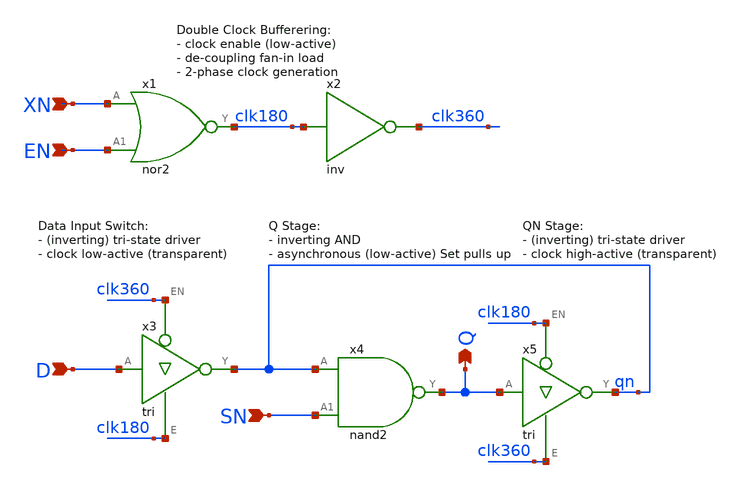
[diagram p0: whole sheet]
** sch_path: Sources/crafted/LATESN.sch
**.subckt LATESN XN D Q EN SN
*.ipin XN
*.ipin D
*.opin Q
*.ipin EN
*.ipin SN
x2 clk180 clk360 VDD GND inv Wmin=1.5u Lmin=1u g=2 m=1
x3 D clk360 clk180 qn VDD GND tri Wmin=1.5u Lmin=1u g=2 m=1
x5 Q clk180 clk360 qn VDD GND tri Wmin=1.5u Lmin=1u g=2 m=1
x1 clk180 XN EN VDD GND nor2 Wmin=1.5u Lmin=1u g=2 m=1
x4 Q qn SN VDD GND nand2 Wmin=1.5u Lmin=1u g=2 m=1
**.ends

* expanding   symbol:  inv.sym # of pins=2
** sym_path: Sources/crafted/inv.sym
** sch_path: Sources/crafted/inv.sch
.subckt inv A Y VDD GND    Wmin=1.5u Lmin=1u g=2
*.ipin A
*.opin Y
m2 Y A GND GND nmos4 w=Wmin l=Lmin m=m
m1 Y A VDD VDD pmos4 w='g*Wmin' l=Lmin m=m
.ends


* expanding   symbol:  tri.sym # of pins=4
** sym_path: Sources/crafted/tri.sym
** sch_path: Sources/crafted/tri.sch
.subckt tri A EN E Y VDD GND    Wmin=1.5u Lmin=1u g=2
*.ipin A
*.iopin Y
*.ipin EN
*.ipin E
m2 Y A net2 GND nmos4 w='2*Wmin' l=Lmin m=m
m1 Y A net1 VDD pmos4 w='2*g*Wmin' l=Lmin m=m
m0 net2 E GND GND nmos4 w='2*Wmin' l=Lmin m=m
m3 net1 EN VDD VDD pmos4 w='2*g*Wmin' l=Lmin m=m
.ends


* expanding   symbol:  nor2.sym # of pins=3
** sym_path: Sources/crafted/nor2.sym
** sch_path: Sources/crafted/nor2.sch
.subckt nor2 Y A A1 VDD GND    Wmin=1.5u Lmin=1u g=2
*.ipin A
*.opin Y
*.ipin A1
m3 Y A GND GND nmos4 w=Wmin l=Lmin m=m
m1 Y A net1 VDD pmos4 w='2*g*Wmin' l=Lmin m=m
m4 Y A1 GND GND nmos4 w=Wmin l=Lmin m=m
m2 net1 A1 VDD VDD pmos4 w='2*g*Wmin' l=Lmin m=m
.ends


* expanding   symbol:  /home/kubrick/Projects/github.com/StdCellLib/Sources/crafted/nand2.sym # of
*+ pins=3
** sym_path: Sources/crafted/nand2.sym
** sch_path: Sources/crafted/nand2.sch
.subckt nand2 Y A A1 VDD GND    Wmin=1.5u Lmin=1u g=2
*.ipin A
*.opin Y
*.ipin A1
m3 Y A net1 GND nmos4 w='2*Wmin' l=Lmin m=m
m1 Y A VDD VDD pmos4 w='g*Wmin' l=Lmin m=m
m4 net1 A1 GND GND nmos4 w='2*Wmin' l=Lmin m=m
m2 Y A1 VDD VDD pmos4 w='g*Wmin' l=Lmin m=m
.ends

.GLOBAL VDD
.GLOBAL GND
.end
